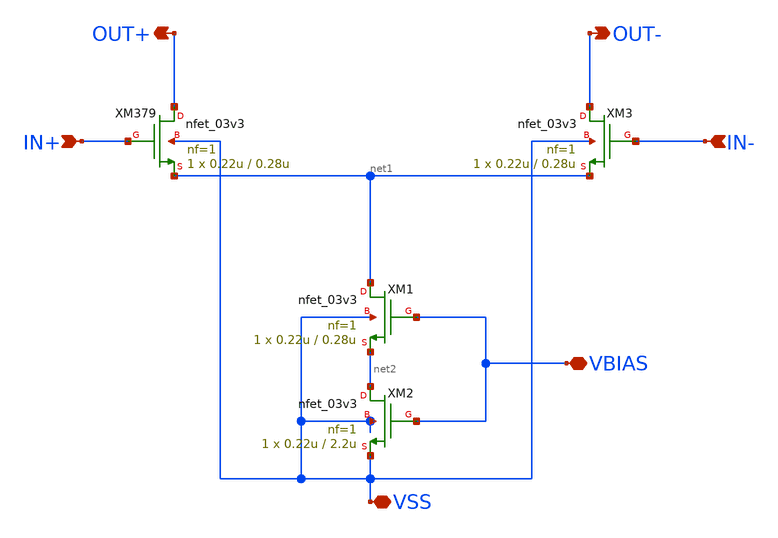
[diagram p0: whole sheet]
** sch_path: xschem/CS_Switch_1x.sch
**.subckt CS_Switch_1x VBIAS IN+ VSS IN- OUT+ OUT-
*.iopin VBIAS
*.ipin IN+
*.iopin VSS
*.ipin IN-
*.opin OUT+
*.opin OUT-
XM379 OUT+ IN+ net1 VSS nfet_03v3 L=0.28u W=0.22u nf=1 ad='int((nf+1)/2) * W/nf * 0.18u' as='int((nf+2)/2) * W/nf * 0.18u'
+ pd='2*int((nf+1)/2) * (W/nf + 0.18u)' ps='2*int((nf+2)/2) * (W/nf + 0.18u)' nrd='0.18u / W' nrs='0.18u / W'
+ sa=0 sb=0 sd=0 m=1
XM3 OUT- IN- net1 VSS nfet_03v3 L=0.28u W=0.22u nf=1 ad='int((nf+1)/2) * W/nf * 0.18u' as='int((nf+2)/2) * W/nf * 0.18u'
+ pd='2*int((nf+1)/2) * (W/nf + 0.18u)' ps='2*int((nf+2)/2) * (W/nf + 0.18u)' nrd='0.18u / W' nrs='0.18u / W'
+ sa=0 sb=0 sd=0 m=1
XM1 net1 VBIAS net2 VSS nfet_03v3 L=0.28u W=0.22u nf=1 ad='int((nf+1)/2) * W/nf * 0.18u' as='int((nf+2)/2) * W/nf * 0.18u'
+ pd='2*int((nf+1)/2) * (W/nf + 0.18u)' ps='2*int((nf+2)/2) * (W/nf + 0.18u)' nrd='0.18u / W' nrs='0.18u / W'
+ sa=0 sb=0 sd=0 m=1
XM2 net2 VBIAS VSS VSS nfet_03v3 L=2.2u W=0.22u nf=1 ad='int((nf+1)/2) * W/nf * 0.18u' as='int((nf+2)/2) * W/nf * 0.18u'
+ pd='2*int((nf+1)/2) * (W/nf + 0.18u)' ps='2*int((nf+2)/2) * (W/nf + 0.18u)' nrd='0.18u / W' nrs='0.18u / W'
+ sa=0 sb=0 sd=0 m=1
**.ends
.end
